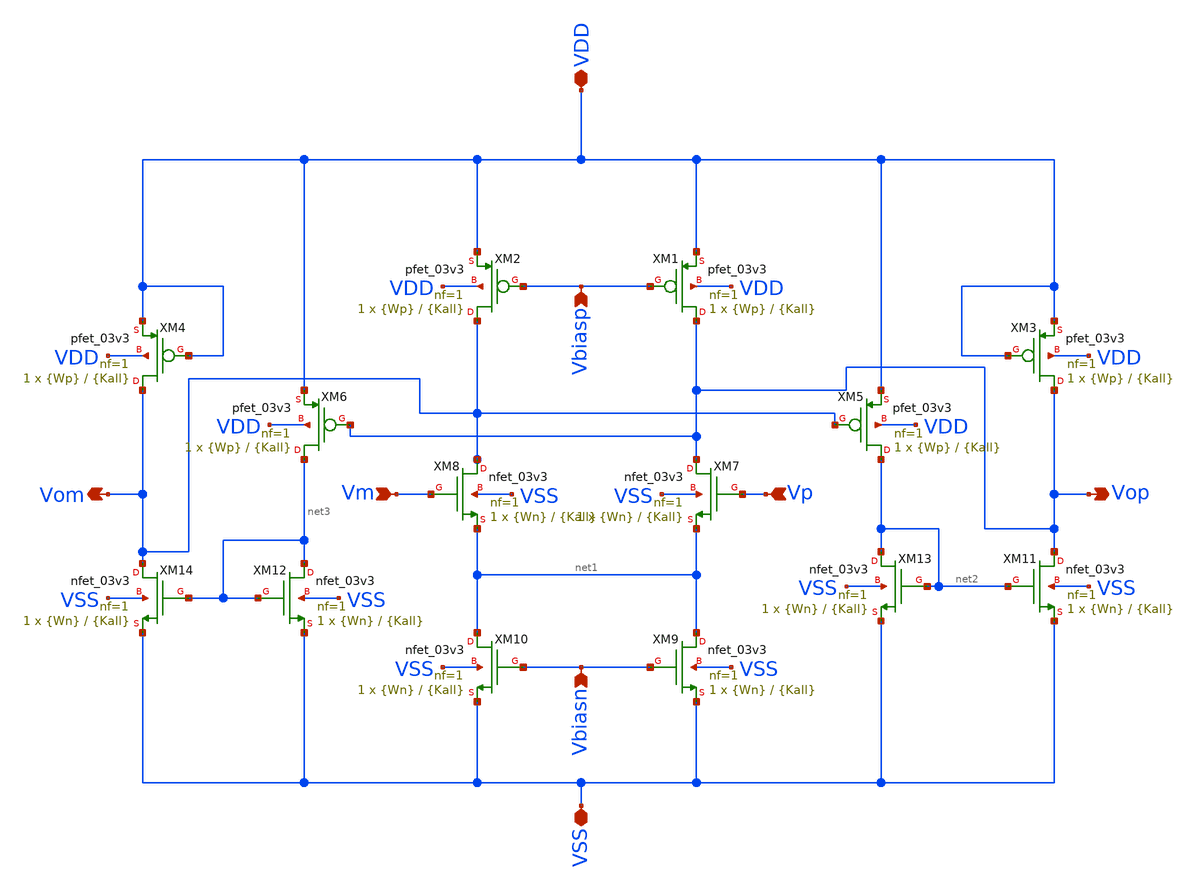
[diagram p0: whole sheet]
** sch_path: src/schematics/TEMPORARY/fulldiffamp.sch
**.subckt fulldiffamp VDD VSS Vbiasn Vbiasp Vm Vp Vom Vop
*.iopin VDD
*.iopin VSS
*.ipin Vbiasn
*.ipin Vbiasp
*.ipin Vm
*.ipin Vp
*.opin Vom
*.opin Vop
XM5 net2 Vom VDD VDD pfet_03v3 L={Kall} W={Wp} nf=1 ad='int((nf+1)/2) * W/nf * 0.18u' as='int((nf+2)/2) * W/nf * 0.18u'
+ pd='2*int((nf+1)/2) * (W/nf + 0.18u)' ps='2*int((nf+2)/2) * (W/nf + 0.18u)' nrd='0.18u / W' nrs='0.18u / W'
+ sa=0 sb=0 sd=0 m=1
XM2 Vom Vbiasp VDD VDD pfet_03v3 L={Kall} W={Wp} nf=1 ad='int((nf+1)/2) * W/nf * 0.18u' as='int((nf+2)/2) * W/nf * 0.18u'
+ pd='2*int((nf+1)/2) * (W/nf + 0.18u)' ps='2*int((nf+2)/2) * (W/nf + 0.18u)' nrd='0.18u / W' nrs='0.18u / W'
+ sa=0 sb=0 sd=0 m=1
XM8 Vom Vm net1 VSS nfet_03v3 L={Kall} W={Wn} nf=1 ad='int((nf+1)/2) * W/nf * 0.18u' as='int((nf+2)/2) * W/nf * 0.18u'
+ pd='2*int((nf+1)/2) * (W/nf + 0.18u)' ps='2*int((nf+2)/2) * (W/nf + 0.18u)' nrd='0.18u / W' nrs='0.18u / W'
+ sa=0 sb=0 sd=0 m=1
XM7 Vop Vp net1 VSS nfet_03v3 L={Kall} W={Wn} nf=1 ad='int((nf+1)/2) * W/nf * 0.18u' as='int((nf+2)/2) * W/nf * 0.18u'
+ pd='2*int((nf+1)/2) * (W/nf + 0.18u)' ps='2*int((nf+2)/2) * (W/nf + 0.18u)' nrd='0.18u / W' nrs='0.18u / W'
+ sa=0 sb=0 sd=0 m=1
XM1 Vop Vbiasp VDD VDD pfet_03v3 L={Kall} W={Wp} nf=1 ad='int((nf+1)/2) * W/nf * 0.18u' as='int((nf+2)/2) * W/nf * 0.18u'
+ pd='2*int((nf+1)/2) * (W/nf + 0.18u)' ps='2*int((nf+2)/2) * (W/nf + 0.18u)' nrd='0.18u / W' nrs='0.18u / W'
+ sa=0 sb=0 sd=0 m=1
XM6 net3 Vop VDD VDD pfet_03v3 L={Kall} W={Wp} nf=1 ad='int((nf+1)/2) * W/nf * 0.18u' as='int((nf+2)/2) * W/nf * 0.18u'
+ pd='2*int((nf+1)/2) * (W/nf + 0.18u)' ps='2*int((nf+2)/2) * (W/nf + 0.18u)' nrd='0.18u / W' nrs='0.18u / W'
+ sa=0 sb=0 sd=0 m=1
XM4 Vom VDD VDD VDD pfet_03v3 L={Kall} W={Wp} nf=1 ad='int((nf+1)/2) * W/nf * 0.18u' as='int((nf+2)/2) * W/nf * 0.18u'
+ pd='2*int((nf+1)/2) * (W/nf + 0.18u)' ps='2*int((nf+2)/2) * (W/nf + 0.18u)' nrd='0.18u / W' nrs='0.18u / W'
+ sa=0 sb=0 sd=0 m=1
XM3 Vop VDD VDD VDD pfet_03v3 L={Kall} W={Wp} nf=1 ad='int((nf+1)/2) * W/nf * 0.18u' as='int((nf+2)/2) * W/nf * 0.18u'
+ pd='2*int((nf+1)/2) * (W/nf + 0.18u)' ps='2*int((nf+2)/2) * (W/nf + 0.18u)' nrd='0.18u / W' nrs='0.18u / W'
+ sa=0 sb=0 sd=0 m=1
XM9 net1 Vbiasn VSS VSS nfet_03v3 L={Kall} W={Wn} nf=1 ad='int((nf+1)/2) * W/nf * 0.18u' as='int((nf+2)/2) * W/nf * 0.18u'
+ pd='2*int((nf+1)/2) * (W/nf + 0.18u)' ps='2*int((nf+2)/2) * (W/nf + 0.18u)' nrd='0.18u / W' nrs='0.18u / W'
+ sa=0 sb=0 sd=0 m=1
XM10 net1 Vbiasn VSS VSS nfet_03v3 L={Kall} W={Wn} nf=1 ad='int((nf+1)/2) * W/nf * 0.18u' as='int((nf+2)/2) * W/nf * 0.18u'
+ pd='2*int((nf+1)/2) * (W/nf + 0.18u)' ps='2*int((nf+2)/2) * (W/nf + 0.18u)' nrd='0.18u / W' nrs='0.18u / W'
+ sa=0 sb=0 sd=0 m=1
XM11 Vop net2 VSS VSS nfet_03v3 L={Kall} W={Wn} nf=1 ad='int((nf+1)/2) * W/nf * 0.18u' as='int((nf+2)/2) * W/nf * 0.18u'
+ pd='2*int((nf+1)/2) * (W/nf + 0.18u)' ps='2*int((nf+2)/2) * (W/nf + 0.18u)' nrd='0.18u / W' nrs='0.18u / W'
+ sa=0 sb=0 sd=0 m=1
XM13 net2 net2 VSS VSS nfet_03v3 L={Kall} W={Wn} nf=1 ad='int((nf+1)/2) * W/nf * 0.18u' as='int((nf+2)/2) * W/nf * 0.18u'
+ pd='2*int((nf+1)/2) * (W/nf + 0.18u)' ps='2*int((nf+2)/2) * (W/nf + 0.18u)' nrd='0.18u / W' nrs='0.18u / W'
+ sa=0 sb=0 sd=0 m=1
XM12 net3 net3 VSS VSS nfet_03v3 L={Kall} W={Wn} nf=1 ad='int((nf+1)/2) * W/nf * 0.18u' as='int((nf+2)/2) * W/nf * 0.18u'
+ pd='2*int((nf+1)/2) * (W/nf + 0.18u)' ps='2*int((nf+2)/2) * (W/nf + 0.18u)' nrd='0.18u / W' nrs='0.18u / W'
+ sa=0 sb=0 sd=0 m=1
XM14 Vom net3 VSS VSS nfet_03v3 L={Kall} W={Wn} nf=1 ad='int((nf+1)/2) * W/nf * 0.18u' as='int((nf+2)/2) * W/nf * 0.18u'
+ pd='2*int((nf+1)/2) * (W/nf + 0.18u)' ps='2*int((nf+2)/2) * (W/nf + 0.18u)' nrd='0.18u / W' nrs='0.18u / W'
+ sa=0 sb=0 sd=0 m=1
**.ends
.end
